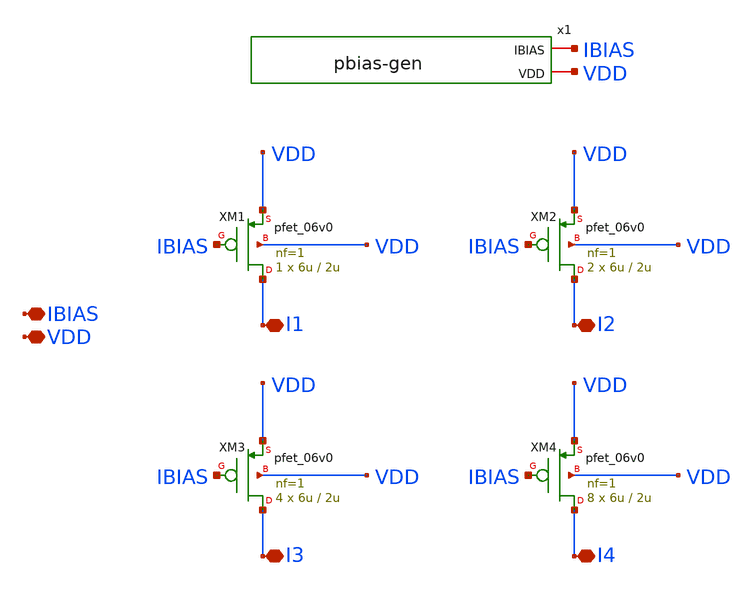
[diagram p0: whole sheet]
** sch_path: designs/libs/core_current-mirror/pmos_current_mirror/pmos_current_mirror.sch
**.subckt pmos_current_mirror IBIAS VDD I1 I2 I3 I4
*.iopin IBIAS
*.iopin VDD
*.iopin I1
*.iopin I2
*.iopin I3
*.iopin I4
x1 IBIAS VDD pbias-gen
XM1 I1 IBIAS VDD VDD pfet_06v0 L=2u W=6u nf=1 ad='int((nf+1)/2) * W/nf * 0.18u' as='int((nf+2)/2) * W/nf * 0.18u'
+ pd='2*int((nf+1)/2) * (W/nf + 0.18u)' ps='2*int((nf+2)/2) * (W/nf + 0.18u)' nrd='0.18u / W' nrs='0.18u / W'
+ sa=0 sb=0 sd=0 m=1
XM2 I2 IBIAS VDD VDD pfet_06v0 L=2u W=6u nf=1 ad='int((nf+1)/2) * W/nf * 0.18u' as='int((nf+2)/2) * W/nf * 0.18u'
+ pd='2*int((nf+1)/2) * (W/nf + 0.18u)' ps='2*int((nf+2)/2) * (W/nf + 0.18u)' nrd='0.18u / W' nrs='0.18u / W'
+ sa=0 sb=0 sd=0 m=2
XM3 I3 IBIAS VDD VDD pfet_06v0 L=2u W=6u nf=1 ad='int((nf+1)/2) * W/nf * 0.18u' as='int((nf+2)/2) * W/nf * 0.18u'
+ pd='2*int((nf+1)/2) * (W/nf + 0.18u)' ps='2*int((nf+2)/2) * (W/nf + 0.18u)' nrd='0.18u / W' nrs='0.18u / W'
+ sa=0 sb=0 sd=0 m=4
XM4 I4 IBIAS VDD VDD pfet_06v0 L=2u W=6u nf=1 ad='int((nf+1)/2) * W/nf * 0.18u' as='int((nf+2)/2) * W/nf * 0.18u'
+ pd='2*int((nf+1)/2) * (W/nf + 0.18u)' ps='2*int((nf+2)/2) * (W/nf + 0.18u)' nrd='0.18u / W' nrs='0.18u / W'
+ sa=0 sb=0 sd=0 m=8
**.ends

* expanding   symbol:  libs/core_current-mirror/pbias-gen/pbias-gen.sym # of pins=2
** sym_path: designs/libs/core_current-mirror/pbias-gen/pbias-gen.sym
** sch_path: designs/libs/core_current-mirror/pbias-gen/pbias-gen.sch
.subckt pbias-gen IBIAS VDD
*.iopin IBIAS
*.iopin VDD
XM1 IBIAS IBIAS VDD VDD pfet_06v0 L=2u W=6u nf=1 ad='int((nf+1)/2) * W/nf * 0.18u' as='int((nf+2)/2) * W/nf * 0.18u'
+ pd='2*int((nf+1)/2) * (W/nf + 0.18u)' ps='2*int((nf+2)/2) * (W/nf + 0.18u)' nrd='0.18u / W' nrs='0.18u / W'
+ sa=0 sb=0 sd=0 m=1
.ends

.end
